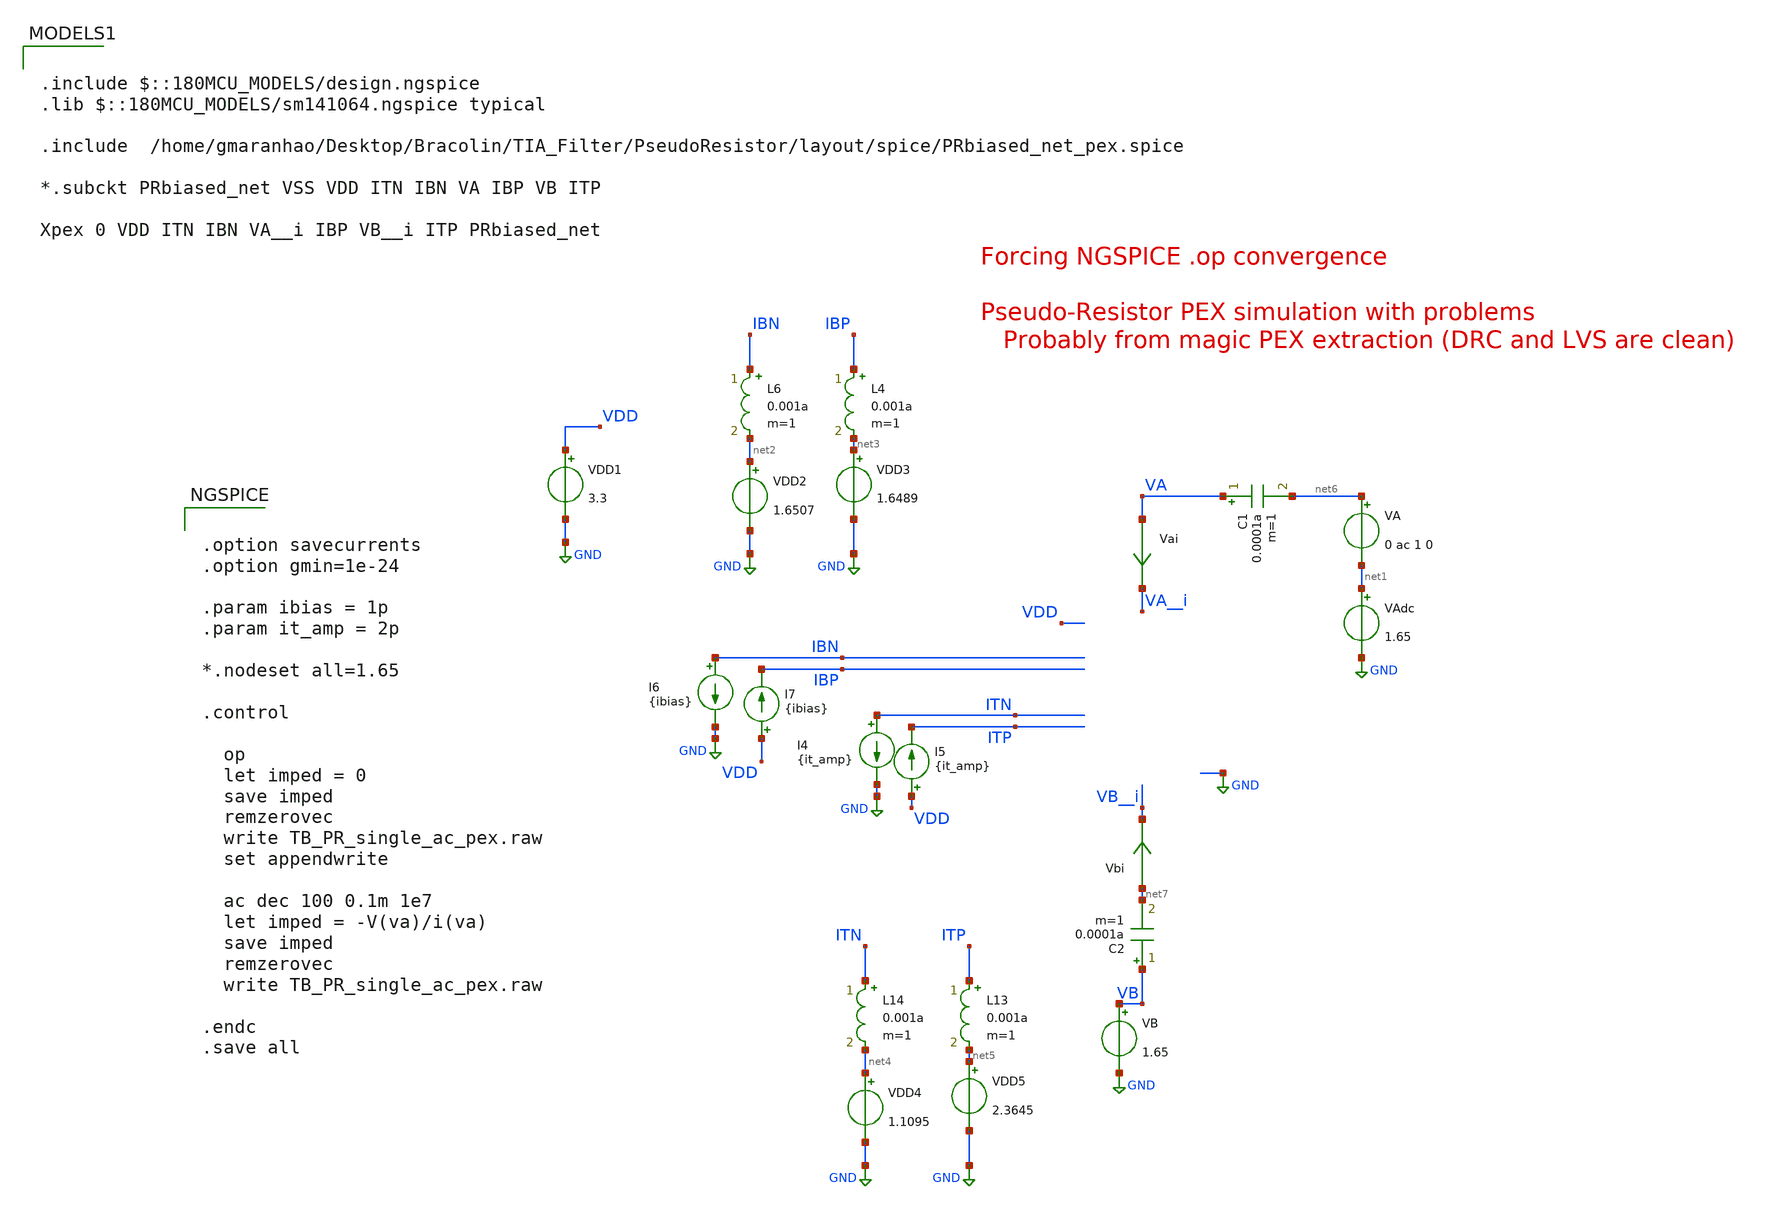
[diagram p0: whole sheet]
** sch_path: TIA_Filter/PseudoResistor/TB_PR_single_ac_pex.sch
**.subckt TB_PR_single_ac_pex
VDD1 VDD GND 3.3
VA net6 net1 0 ac 1 0
VB VB GND 1.65
VAdc net1 GND 1.65
I4 ITN GND {it_amp}
I5 VDD ITP {it_amp}
I6 IBN GND {ibias}
I7 VDD IBP {ibias}
Vai VA VA__i 0
.save i(vai)
Vbi net7 VB__i 0
.save i(vbi)
VDD2 net2 GND 1.6507
VDD3 net3 GND 1.6489
L4 IBP net3 0.001a m=1
L6 IBN net2 0.001a m=1
VDD4 net4 GND 1.1095
VDD5 net5 GND 2.3645
L13 ITP net5 0.001a m=1
L14 ITN net4 0.001a m=1
C1 VA net6 0.0001a m=1
C2 VB net7 0.0001a m=1
**** begin user architecture code


.option savecurrents
.option gmin=1e-24

.param ibias = 1p
.param it_amp = 2p

*.nodeset all=1.65

.control

  op
  let imped = 0
  save imped
  remzerovec
  write TB_PR_single_ac_pex.raw
  set appendwrite

  ac dec 100 0.1m 1e7
  let imped = -V(va)/i(va)
  save imped
  remzerovec
  write TB_PR_single_ac_pex.raw

.endc
.save all



.include $::180MCU_MODELS/design.ngspice
.lib $::180MCU_MODELS/sm141064.ngspice typical

.include  /home/gmaranhao/Desktop/Bracolin/TIA_Filter/PseudoResistor/layout/spice/PRbiased_net_pex.spice

*.subckt PRbiased_net VSS VDD ITN IBN VA IBP VB ITP

Xpex 0 VDD ITN IBN VA__i IBP VB__i ITP PRbiased_net


**** end user architecture code
**.ends
.GLOBAL GND
.end
